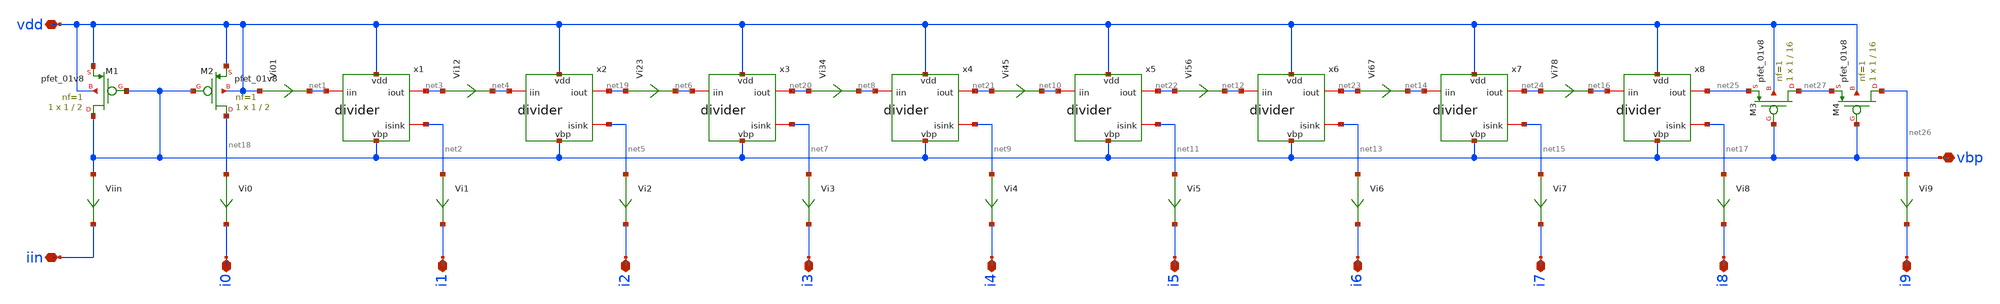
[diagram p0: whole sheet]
** sch_path: xschem/dividerchain.sch
**.subckt dividerchain vdd iin vbp i0 i1 i2 i3 i4 i5 i6 i7 i8 i9
*.iopin vdd
*.iopin iin
*.iopin vbp
*.iopin i0
*.iopin i1
*.iopin i2
*.iopin i3
*.iopin i4
*.iopin i5
*.iopin i6
*.iopin i7
*.iopin i8
*.iopin i9
Viin vbp iin 0
.save i(viin)
Vi0 net18 i0 0
.save i(vi0)
Vi01 vdd net1 0
.save i(vi01)
Vi1 net2 i1 0
.save i(vi1)
Vi12 net3 net4 0
.save i(vi12)
Vi2 net5 i2 0
.save i(vi2)
Vi23 net19 net6 0
.save i(vi23)
Vi3 net7 i3 0
.save i(vi3)
Vi34 net20 net8 0
.save i(vi34)
Vi4 net9 i4 0
.save i(vi4)
Vi45 net21 net10 0
.save i(vi45)
Vi5 net11 i5 0
.save i(vi5)
Vi56 net22 net12 0
.save i(vi56)
Vi6 net13 i6 0
.save i(vi6)
Vi67 net23 net14 0
.save i(vi67)
Vi7 net15 i7 0
.save i(vi7)
Vi78 net24 net16 0
.save i(vi78)
Vi8 net17 i8 0
.save i(vi8)
Vi9 net26 i9 0
.save i(vi9)
x1 vdd net1 net3 vbp net2 divider
x2 vdd net4 net19 vbp net5 divider
x3 vdd net6 net20 vbp net7 divider
x4 vdd net8 net21 vbp net9 divider
x5 vdd net10 net22 vbp net11 divider
x6 vdd net12 net23 vbp net13 divider
x7 vdd net14 net24 vbp net15 divider
x8 vdd net16 net25 vbp net17 divider
XM1 vbp vbp vdd vdd sky130_fd_pr__pfet_01v8 L=2 W=1 nf=1 ad='int((nf+1)/2) * W/nf * 0.29' as='int((nf+2)/2) * W/nf * 0.29'
+ pd='2*int((nf+1)/2) * (W/nf + 0.29)' ps='2*int((nf+2)/2) * (W/nf + 0.29)' nrd='0.29 / W' nrs='0.29 / W'
+ sa=0 sb=0 sd=0 mult=1 m=1
XM2 net18 vbp vdd vdd sky130_fd_pr__pfet_01v8 L=2 W=1 nf=1 ad='int((nf+1)/2) * W/nf * 0.29' as='int((nf+2)/2) * W/nf * 0.29'
+ pd='2*int((nf+1)/2) * (W/nf + 0.29)' ps='2*int((nf+2)/2) * (W/nf + 0.29)' nrd='0.29 / W' nrs='0.29 / W'
+ sa=0 sb=0 sd=0 mult=1 m=1
XM3 net27 vbp net25 vdd sky130_fd_pr__pfet_01v8 L=16 W=1 nf=1 ad='int((nf+1)/2) * W/nf * 0.29' as='int((nf+2)/2) * W/nf * 0.29'
+ pd='2*int((nf+1)/2) * (W/nf + 0.29)' ps='2*int((nf+2)/2) * (W/nf + 0.29)' nrd='0.29 / W' nrs='0.29 / W'
+ sa=0 sb=0 sd=0 mult=1 m=1
XM4 net26 vbp net27 vdd sky130_fd_pr__pfet_01v8 L=16 W=1 nf=1 ad='int((nf+1)/2) * W/nf * 0.29' as='int((nf+2)/2) * W/nf * 0.29'
+ pd='2*int((nf+1)/2) * (W/nf + 0.29)' ps='2*int((nf+2)/2) * (W/nf + 0.29)' nrd='0.29 / W' nrs='0.29 / W'
+ sa=0 sb=0 sd=0 mult=1 m=1
**.ends

* expanding   symbol:  divider.sym # of pins=5
** sym_path: divider.sym
** sch_path: divider.sch
.subckt divider vdd iin iout vbp isink
*.iopin iin
*.iopin vdd
*.iopin vbp
*.iopin iout
*.iopin isink
XM12 ds vbp net1 vdd sky130_fd_pr__pfet_01v8 L=15.5 W=1 nf=1 ad='int((nf+1)/2) * W/nf * 0.29' as='int((nf+2)/2) * W/nf * 0.29'
+ pd='2*int((nf+1)/2) * (W/nf + 0.29)' ps='2*int((nf+2)/2) * (W/nf + 0.29)' nrd='0.29 / W' nrs='0.29 / W'
+ sa=0 sb=0 sd=0 mult=1 m=1
Viin iin net1 0
.save i(viin)
Viout node iout 0
.save i(viout)
XM1 net2 vbp node vdd sky130_fd_pr__pfet_01v8 L=2 W=1 nf=1 ad='int((nf+1)/2) * W/nf * 0.29' as='int((nf+2)/2) * W/nf * 0.29'
+ pd='2*int((nf+1)/2) * (W/nf + 0.29)' ps='2*int((nf+2)/2) * (W/nf + 0.29)' nrd='0.29 / W' nrs='0.29 / W'
+ sa=0 sb=0 sd=0 mult=1 m=1
Visink net2 isink 0
.save i(visink)
XM2 node vbp ds vdd sky130_fd_pr__pfet_01v8 L=15.5 W=1 nf=1 ad='int((nf+1)/2) * W/nf * 0.29' as='int((nf+2)/2) * W/nf * 0.29'
+ pd='2*int((nf+1)/2) * (W/nf + 0.29)' ps='2*int((nf+2)/2) * (W/nf + 0.29)' nrd='0.29 / W' nrs='0.29 / W'
+ sa=0 sb=0 sd=0 mult=1 m=1
.ends

.end
